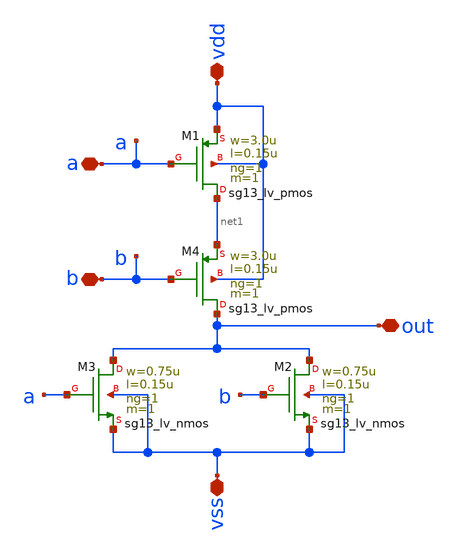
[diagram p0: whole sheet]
** sch_path: design/blocks/norgate/schematic/nor.sch
**.subckt nor vdd a vss out b
*.iopin vdd
*.iopin a
*.iopin vss
*.iopin out
*.iopin b
XM1 net1 a vdd vdd sg13_lv_pmos w=3.0u l=0.15u ng=1 m=1 mm_ok=1
XM2 out b vss vss sg13_lv_nmos w=0.75u l=0.15u ng=1 m=1 mm_ok=1
XM3 out a vss vss sg13_lv_nmos w=0.75u l=0.15u ng=1 m=1 mm_ok=1
XM4 out b net1 vdd sg13_lv_pmos w=3.0u l=0.15u ng=1 m=1 mm_ok=1
**.ends
.end
